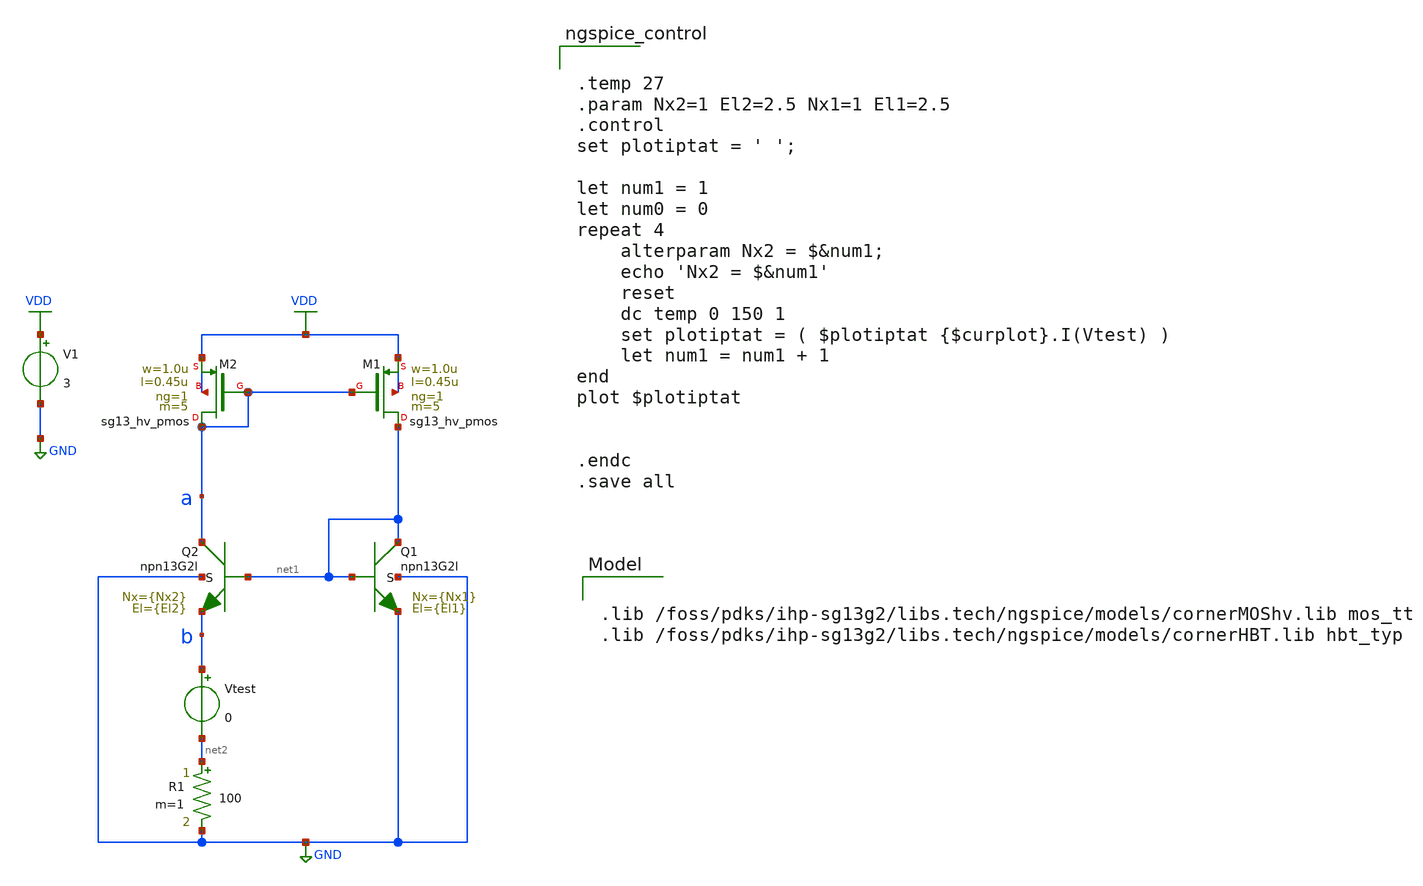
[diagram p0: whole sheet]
** sch_path: data_simu/simulations/curr_mirror.sch
**.subckt curr_mirror
XM1 net1 a VDD VDD sg13_hv_pmos w=1.0u l=0.45u ng=1 m=5 mm_ok=1
XM2 a a VDD VDD sg13_hv_pmos w=1.0u l=0.45u ng=1 m=5 mm_ok=1
R1 net2 GND 100 m=1
V1 VDD GND 3
XQ1 net1 net1 GND GND npn13G2l Nx={Nx1} El={El1} mm_ok=1
XQ2 a net1 b GND npn13G2l Nx={Nx2} El={El2} mm_ok=1
Vtest b net2 0
**** begin user architecture code


.lib /foss/pdks/ihp-sg13g2/libs.tech/ngspice/models/cornerMOShv.lib mos_tt
.lib /foss/pdks/ihp-sg13g2/libs.tech/ngspice/models/cornerHBT.lib hbt_typ




.temp 27
.param Nx2=1 El2=2.5 Nx1=1 El1=2.5
.control
set plotiptat = ' ';

let num1 = 1
let num0 = 0
repeat 4
	alterparam Nx2 = $&num1;
	echo 'Nx2 = $&num1'
	reset
	dc temp 0 150 1
	set plotiptat = ( $plotiptat {$curplot}.I(Vtest) )
	let num1 = num1 + 1
end
plot $plotiptat


.endc
.save all


**** end user architecture code
**.ends
.GLOBAL VDD
.GLOBAL GND
.end
